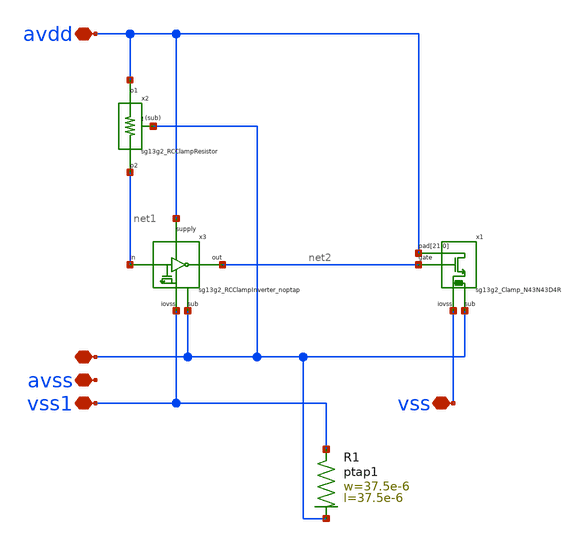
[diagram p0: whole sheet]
** sch_path: MSPHY6034-main/dependencies/unic_cass_2025_team04_padring/xschem/openpdk-libraries/ihp-sg13g2/sg13g2_io/xschem/sg13g2_IOPadAVdd.sch
**.subckt sg13g2_IOPadAVdd avdd avss ! vss1 vss
*.iopin avdd
*.iopin avss
*.iopin !
*.iopin vss1
*.iopin vss
XR1 vss1 ! ptap1 R=629.7m w=37.5e-6 l=37.5e-6
x1 vss avdd avdd avdd avdd avdd avdd avdd avdd avdd avdd avdd avdd avdd avdd avdd avdd avdd avdd
+ avdd avdd avdd avdd ! net2 sg13g2_Clamp_N43N43D4R
x2 avdd net1 ! sg13g2_RCClampResistor
x3 avdd vss1 net1 net2 ! sg13g2_RCClampInverter_noptap
**.ends
.end
